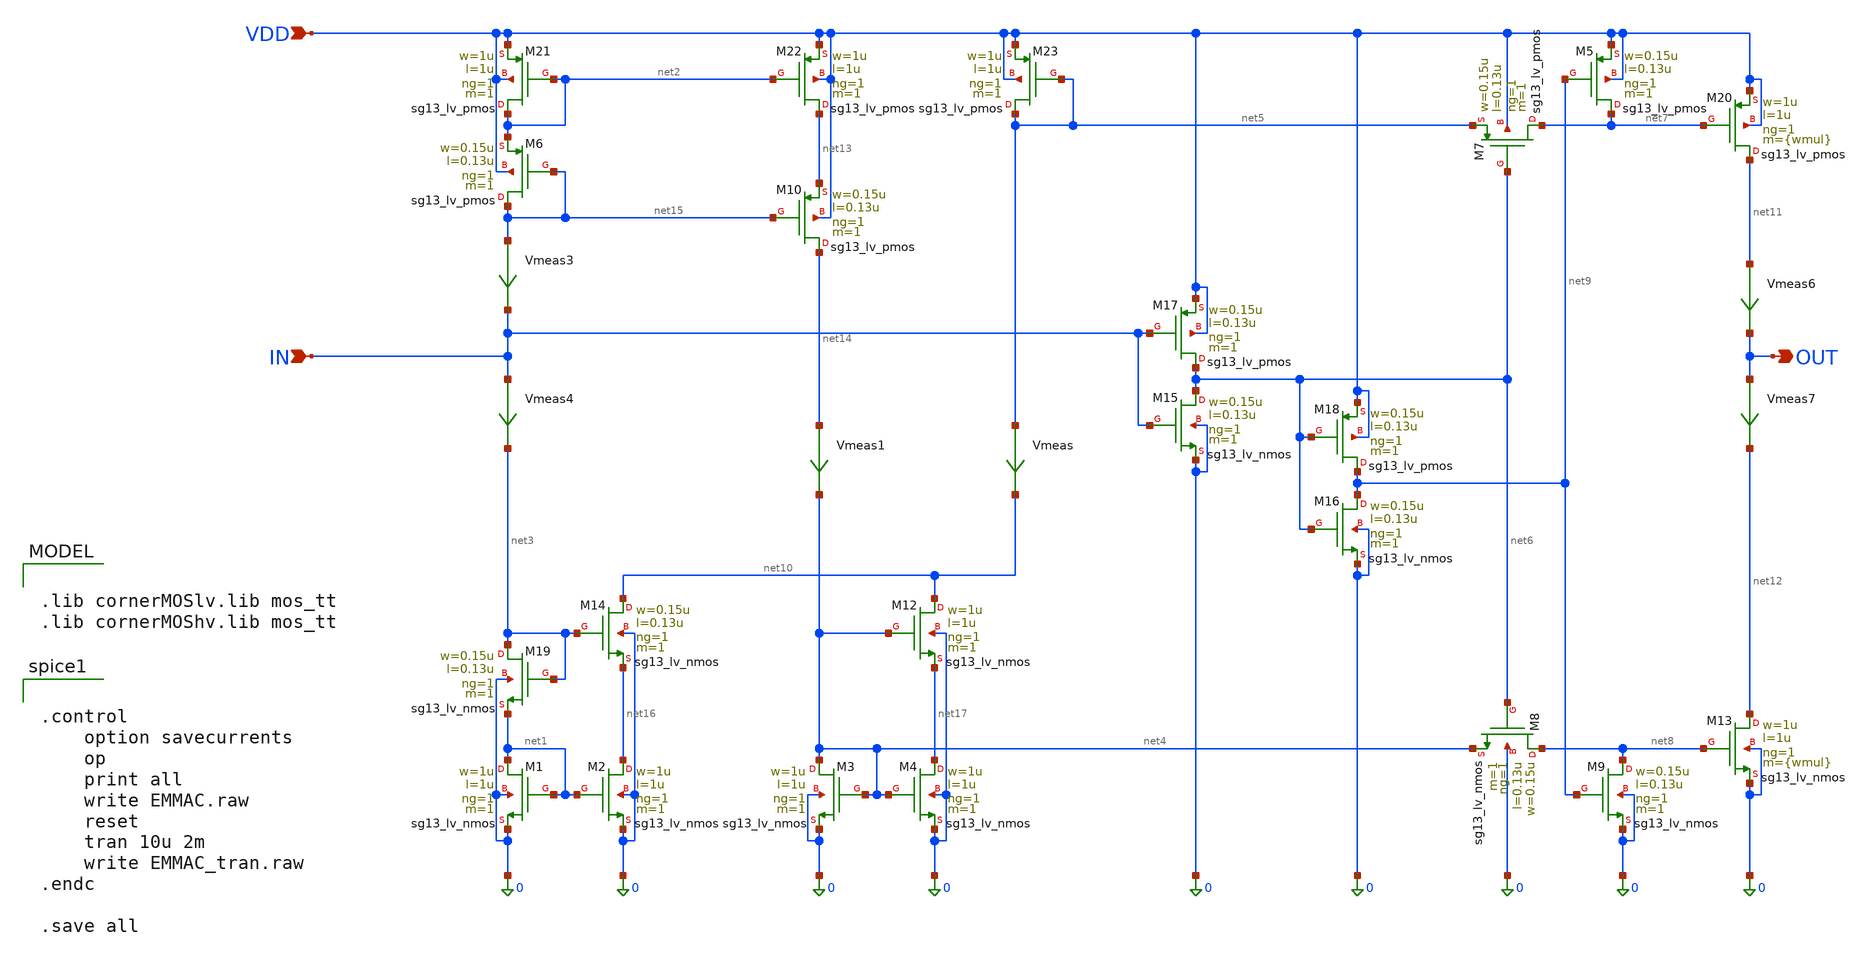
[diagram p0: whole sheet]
** sch_path: src/analog_mac/EMMAC_Block_v3.sch
**.subckt EMMAC_Block_v3 OUT IN VDD
*.opin OUT
*.ipin IN
*.ipin VDD
XM1 net1 net1 0 0 sg13_lv_nmos w=1u l=1u ng=1 m=1 mm_ok=1
XM2 net16 net1 0 0 sg13_lv_nmos w=1u l=1u ng=1 m=1 mm_ok=1
XM21 net2 net2 VDD VDD sg13_lv_pmos w=1u l=1u ng=1 m=1 mm_ok=1
XM22 net13 net2 VDD VDD sg13_lv_pmos w=1u l=1u ng=1 m=1 mm_ok=1
XM3 net4 net4 0 0 sg13_lv_nmos w=1u l=1u ng=1 m=1 mm_ok=1
XM4 net17 net4 0 0 sg13_lv_nmos w=1u l=1u ng=1 m=1 mm_ok=1
XM23 net5 net5 VDD VDD sg13_lv_pmos w=1u l=1u ng=1 m=1 mm_ok=1
XM20 net11 net7 VDD VDD sg13_lv_pmos w=1u l=1u ng=1 m={wmul} mm_ok=1
XM13 net12 net8 0 0 sg13_lv_nmos w=1u l=1u ng=1 m={wmul} mm_ok=1
XM15 net6 IN 0 0 sg13_lv_nmos w=0.15u l=0.13u ng=1 m=1 mm_ok=1
XM17 net6 IN VDD VDD sg13_lv_pmos w=0.15u l=0.13u ng=1 m=1 mm_ok=1
XM16 net9 net6 0 0 sg13_lv_nmos w=0.15u l=0.13u ng=1 m=1 mm_ok=1
XM18 net9 net6 VDD VDD sg13_lv_pmos w=0.15u l=0.13u ng=1 m=1 mm_ok=1
Vmeas net5 net10 0
.save i(vmeas)
Vmeas3 net15 IN 0
.save i(vmeas3)
Vmeas4 IN net3 0
.save i(vmeas4)
Vmeas6 net11 OUT 0
.save i(vmeas6)
Vmeas7 OUT net12 0
.save i(vmeas7)
XM19 net3 net3 net1 0 sg13_lv_nmos w=0.15u l=0.13u ng=1 m=1 mm_ok=1
Vmeas1 net14 net4 0
.save i(vmeas1)
XM7 net7 net6 net5 VDD sg13_lv_pmos w=0.15u l=0.13u ng=1 m=1 mm_ok=1
XM5 net7 net9 VDD VDD sg13_lv_pmos w=0.15u l=0.13u ng=1 m=1 mm_ok=1
XM8 net8 net6 net4 0 sg13_lv_nmos w=0.15u l=0.13u ng=1 m=1 mm_ok=1
XM9 net8 net9 0 0 sg13_lv_nmos w=0.15u l=0.13u ng=1 m=1 mm_ok=1
XM14 net10 net3 net16 0 sg13_lv_nmos w=0.15u l=0.13u ng=1 m=1 mm_ok=1
XM6 net15 net15 net2 VDD sg13_lv_pmos w=0.15u l=0.13u ng=1 m=1 mm_ok=1
XM12 net10 net4 net17 0 sg13_lv_nmos w=1u l=1u ng=1 m=1 mm_ok=1
XM10 net14 net15 net13 VDD sg13_lv_pmos w=0.15u l=0.13u ng=1 m=1 mm_ok=1
**** begin user architecture code

.lib cornerMOSlv.lib mos_tt
.lib cornerMOShv.lib mos_tt



.control
	option savecurrents
	op
	print all
	write EMMAC.raw
	reset
	tran 10u 2m
	write EMMAC_tran.raw
.endc

.save all


**** end user architecture code
**.ends
.end
